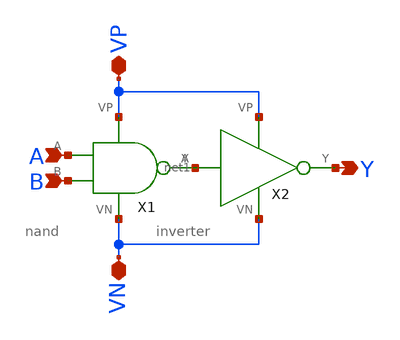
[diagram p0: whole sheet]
** sch_path: lib/digital/schematic/and.sch
**.subckt and A B VP VN Y
*.ipin A
*.ipin B
*.iopin VP
*.iopin VN
*.opin Y
X1 A net1 VP VN B nand
X2 net1 Y VP VN inverter
**.ends
.end
